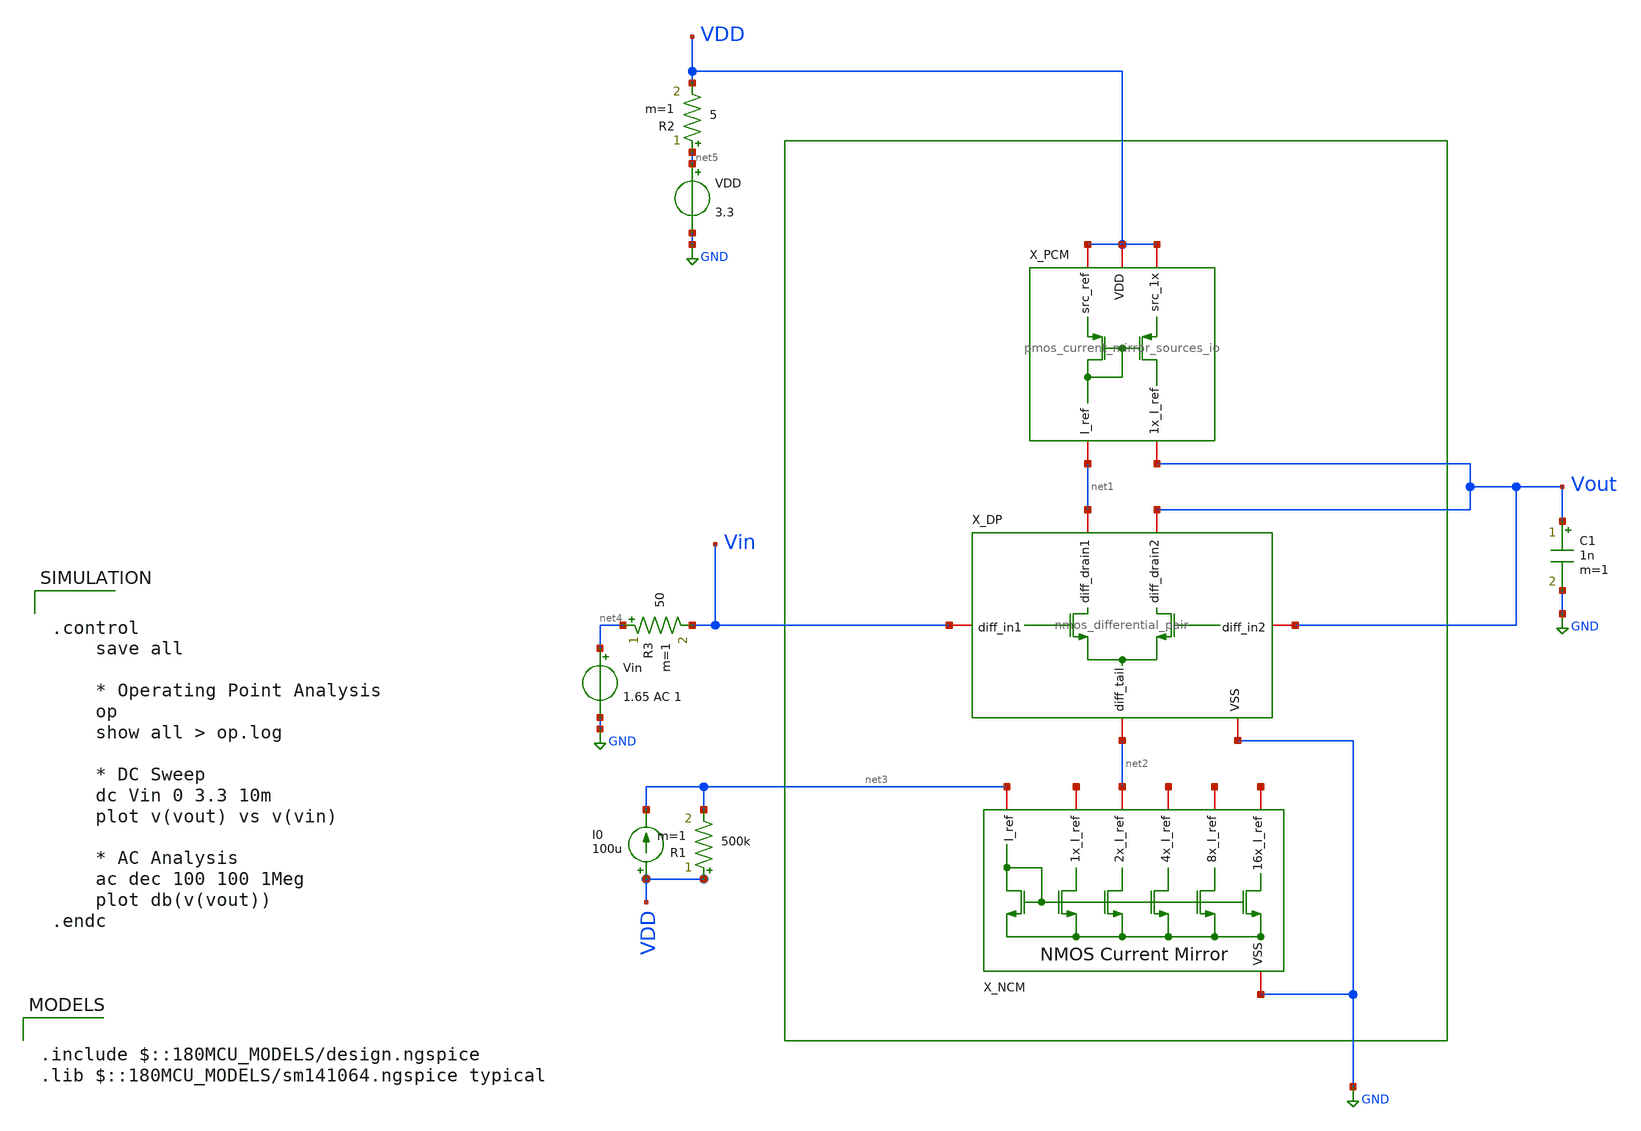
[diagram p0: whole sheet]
** sch_path: designs/libs/tb_applications/tb_5t_ota/tb_5t_ota.sch
**.subckt tb_5t_ota
X_DP net1 Vout GND Vout Vin net2 nmos_differential_pair
X_NCM net6 net7 net8 net2 net9 net3 GND nmos_current_mirror
X_PCM VDD VDD Vout net1 VDD pmos_current_mirror_sources_io
VDD net5 GND 3.3
I0 VDD net3 100u
Vin net4 GND 1.65 AC 1
R1 VDD net3 500k m=1
R2 net5 VDD 5 m=1
C1 Vout GND 1n m=1
R3 net4 Vin 50 m=1
**** begin user architecture code

.include $::180MCU_MODELS/design.ngspice
.lib $::180MCU_MODELS/sm141064.ngspice typical



.control
    save all

    * Operating Point Analysis
    op
    show all > op.log

    * DC Sweep
    dc Vin 0 3.3 10m
    plot v(vout) vs v(vin)

    * AC Analysis
    ac dec 100 100 1Meg
    plot db(v(vout))
.endc


**** end user architecture code
**.ends
.GLOBAL GND
.end
